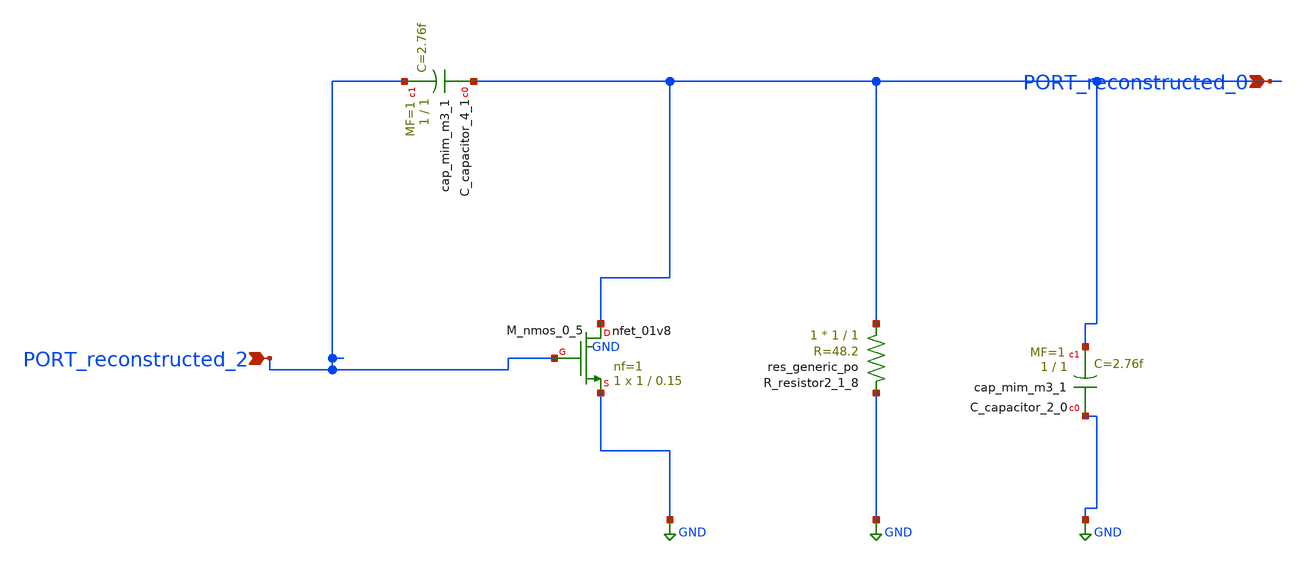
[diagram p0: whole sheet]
** sch_path: schematics/AMSNet/388.sch
**.subckt 388 PORT_reconstructed_2 PORT_reconstructed_0
*.ipin PORT_reconstructed_2
*.ipin PORT_reconstructed_0
XC_capacitor_2_0 GND PORT_reconstructed_0 sky130_fd_pr__cap_mim_m3_1 W=1 L=1 MF=1 m=1
XC_capacitor_4_1 PORT_reconstructed_0 PORT_reconstructed_2 sky130_fd_pr__cap_mim_m3_1 W=1 L=1 MF=1
+ m=1
XM_nmos_0_5 PORT_reconstructed_0 PORT_reconstructed_2 GND GND sky130_fd_pr__nfet_01v8 L=0.15 W=1 nf=1
+ ad='int((1 + 1)/2) * 1 / 1 * 0.29' as='int((1 + 2)/2) * 1 / 1 * 0.29' pd='2*int((1 + 1)/2) * (1 / 1 + 0.29)'
+ ps='2*int((1 + 2)/2) * (1 / 1 + 0.29)' nrd='0.29 / 1 ' nrs='0.29 / 1 ' sa=0 sb=0 sd=0 mult=1 m=1
XR_resistor2_1_8 PORT_reconstructed_0 GND sky130_fd_pr__res_generic_po W=1 L=1 m=1
**.ends
.GLOBAL GND
.end
